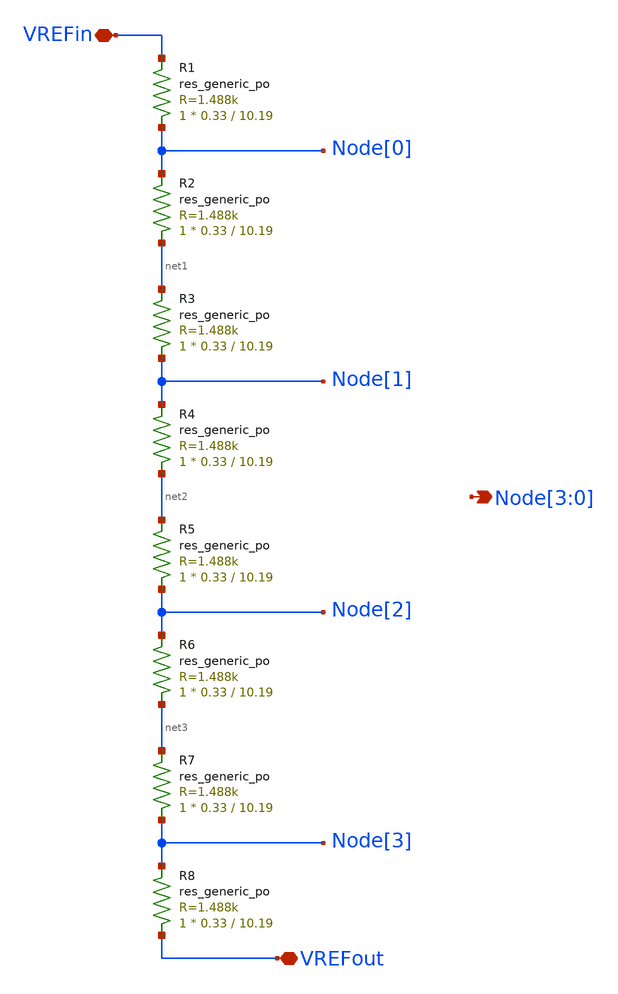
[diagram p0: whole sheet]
** sch_path: sky130_cells/RDAC/Design/sky130_hilas_resistor_string.sch
**.subckt sky130_hilas_resistor_string VREFout VREFin Node[3],Node[2],Node[1],Node[0]
*.iopin VREFout
*.iopin VREFin
*.opin Node[3],Node[2],Node[1],Node[0]
XR1 Node[0] VREFin sky130_fd_pr__res_generic_po W=0.33 L=10.19 m=1
XR2 net1 Node[0] sky130_fd_pr__res_generic_po W=0.33 L=10.19 m=1
XR3 Node[1] net1 sky130_fd_pr__res_generic_po W=0.33 L=10.19 m=1
XR4 net2 Node[1] sky130_fd_pr__res_generic_po W=0.33 L=10.19 m=1
XR5 Node[2] net2 sky130_fd_pr__res_generic_po W=0.33 L=10.19 m=1
XR6 net3 Node[2] sky130_fd_pr__res_generic_po W=0.33 L=10.19 m=1
XR7 Node[3] net3 sky130_fd_pr__res_generic_po W=0.33 L=10.19 m=1
XR8 VREFout Node[3] sky130_fd_pr__res_generic_po W=0.33 L=10.19 m=1
**.ends
.end
